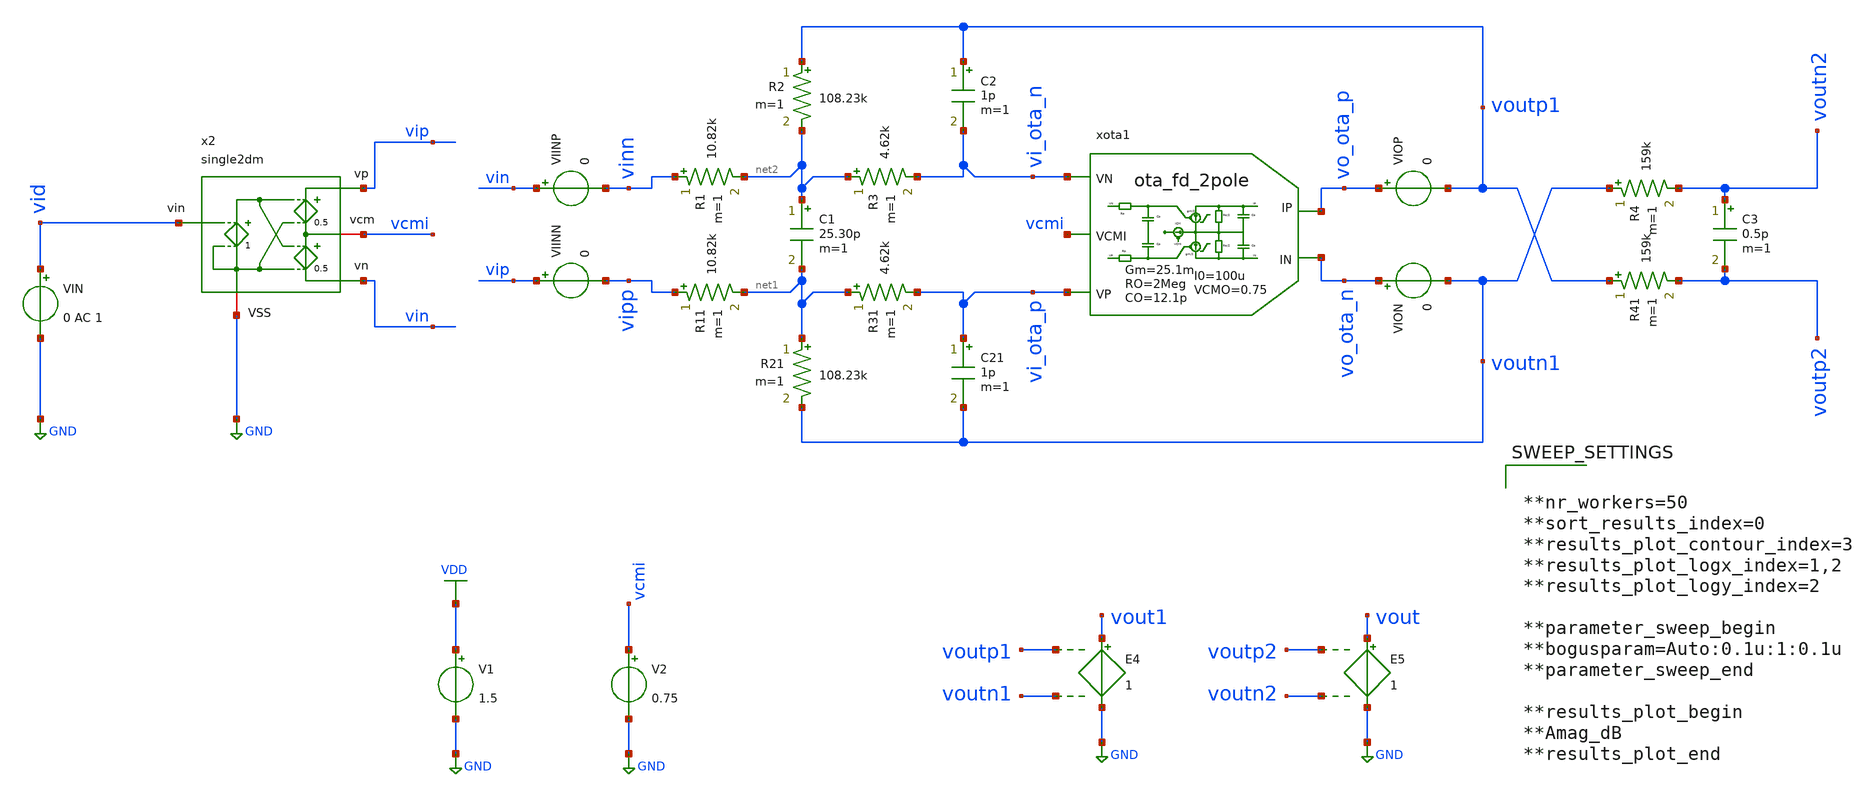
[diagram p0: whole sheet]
** sch_path: macros/filter_cmos5l/testbenches/xschem/filter_cl_ideal_tb.sch
**.subckt filter_cl_ideal_tb
VIN vid GND 0 AC 1
E4 vout1 GND voutp1 voutn1 1
VIINP vin vinn 0
VIINN vip vipp 0
R1 vinn net2 10.82k m=1
R2 voutp1 net2 108.23k m=1
R3 net2 vi_ota_n 4.62k m=1
C1 net2 net1 25.30p m=1
C3 voutn2 voutp2 0.5p m=1
R11 vipp net1 10.82k m=1
R21 net1 voutn1 108.23k m=1
R31 net1 vi_ota_p 4.62k m=1
C21 vi_ota_p voutn1 1p m=1
R4 voutn1 voutn2 159k m=1
R41 voutp1 voutp2 159k m=1
C2 voutp1 vi_ota_n 1p m=1
E5 vout GND voutp2 voutn2 1
VIOP vo_ota_p voutp1 0
VION vo_ota_n voutn1 0
V1 VDD GND 1.5
x2 vip vid vcmi GND vin single2dm
V2 vcmi GND 0.75
xota1 vi_ota_n vo_ota_p vo_ota_n vi_ota_p vcmi ota_fd_2pole GM=25.1m RO=2Meg CO=12.1p RP=0 CP=0.1p
+ VCMO=0.75 I0=100u
**** begin user architecture code


.options savecurrents
.options method=gear reltol=.005
.options sparse
.control
save all

let f_min = 10
let f_max = 100Meg
let f_stop = 9Meg
let f_nmin = 100
let f_nmax = 5Meg

let n_bits = 8
let Adc = 10
let v_fs = 1.0
let v_lsb = v_fs/2^n_bits
let v_qn = v_lsb/sqrt(12)
let err_gain_spec = v_lsb/v_fs
let vo_n_max = 113e-6

let v_step_o = v_fs
let v_step_i = v_step_o/Adc

let t_rf = 0.1u
let t_step = 50u
let t_delay = 0
let t_per = 2*t_step

let tstep = 0.1*t_rf
let tstop = 2*t_per
let tstart = t_delay

*alter @VIN[SIN] = [ 0 0.01 $&f_sig 0 0 0 ]
alter @VIN[DC] = 0.0

set wr_singlescale
set wr_vecnames
option numdgt=3

set opSimOnly = 0


** Main Simulations
if $opSimOnly eq 0
	op
	ac dec 100 $&const.f_min $&const.f_max
	*set sqrnoise
	noise v(vout) VIN dec 100 $&const.f_min $&const.f_max 1
	noise v(vout) VIN dec 10 $&const.f_nmin $&const.f_nmax
	alter @VIN[PULSE] = [ 0 $&v_step_i $&t_delay $&t_rf $&t_rf $&t_step $&t_per 0 ]
	** Check power on by ramping Vdd, tie di_pon to VDD net!
	*alter @V1[PULSE] = [ 0 1.8 0 10u $&t_rf 0 0 0 ]
	tran $&tstep $&tstop $&tstart

	setplot ac1
	let A1 = v(vout1)/v(vid)
	let A2 = v(vout)/v(vid)

	let Amag_dB = vdb(A2)
	settype decibel Amag_dB
	let Aarg = 180/PI*cphase(A2)
	echo results_plot_begin
	print Amag_dB
	echo results_plot_end
	let fdc = const.f_min+1
	meas ac Adc_ol_dB find Amag_dB when frequency = fdc
	let Amag_fc = Adc_ol_dB-3
	meas ac fc find frequency when Amag_dB = Amag_fc
	meas ac Amin min_at Amag_dB from=const.f_min to=fc
	meas ac Amax max Amag_dB
	meas ac Astop find Amag_dB when frequency = const.f_stop
	let att_db = Adc_ol_dB-Astop

	meas ac fug find frequency when Amag_dB=0
	let err_gain_act = 1-10^(Adc_ol_dB/20)/Adc
	let Adc_ol_min = (1+Adc)*(1-err_gain_spec)/err_gain_spec
	let Adc_ol_min_dB = vdb(Adc_ol_min)
	print err_gain_act*100
	print Adc_ol_min_dB
	print att_db
	wrdata ../plot_simulations/data/filter_cl_ideal_tb_ac.txt Amag_dB Aarg
	plot Amag_dB Aarg ylabel 'Magnitude, Phase'

	setplot noise3
	wrdata ../plot_simulations/data/filter_cl_ideal_tb_noise.txt onoise_spectrum

	setplot noise4
	let p_noise_q = const.v_qn^2
	let p_noise_o = onoise_total^2
	let p_sig_o = (v_step_o/(2*sqrt(2)))^2
	let snr = p_sig_o/(p_noise_o+p_noise_q)
	let snr_dB = 10*log10(snr)
	print snr_dB

	setplot tran4
	let vid = v(vid)
	let iop = viop#branch
	let ion = vion#branch
	let vcmo = (voutp1+voutn1)/2

	*plot iop ion

	*plot vid vout1 vout vcmo
	*plot v(vip) v(vin) v(voutp1) v(voutn1) vcmo
end

alter @VIN[DC] = 0
op

remzerovec
write filter_cl_ideal_tb.raw
.endc



**nr_workers=50
**sort_results_index=0
**results_plot_contour_index=3
**results_plot_logx_index=1,2
**results_plot_logy_index=2

**parameter_sweep_begin
**bogusparam=Auto:0.1u:1:0.1u
**parameter_sweep_end

**results_plot_begin
**Amag_dB
**results_plot_end


**** end user architecture code
**.ends

* expanding   symbol:  single2dm.sym # of pins=5
** sym_path: single2dm.sym
** sch_path: single2dm.sch
.subckt single2dm vp vin vcm VSS vn
*.ipin vin
*.opin vn
*.iopin vcm
*.opin vp
*.iopin VSS
E3 vcm vn net1 VSS 0.5
E2 vp vcm net1 VSS 0.5
E1 net1 VSS vin VSS 1
.ends


* expanding   symbol:  ota_fd_2pole.sym # of pins=5
** sym_path: ota_fd_2pole.sym
** sch_path: ota_fd_2pole.sch
.subckt ota_fd_2pole VN IP IN VP VCMI  GM=1u RO=100Meg CO=1p RP=0 CP=0.1p VCMO=0 I0=1u
*.ipin VP
*.ipin VN
*.opin IP
*.opin IN
*.ipin VCMI
R3 IP net1 {RO/2} m=1
R4 IN net1 {RO/2} m=1
C3 IP net1 {CO} m=1
R5 VN ip1 {RP} m=1
C4 ip1 VCMI {CP} m=1
C6 in1 VCMI {CP} m=1
C8 IN net1 {CO} m=1
R7 VP in1 {RP} m=1
B2 IP net1 I = {I0*tanh(GM/2*V(ip1,in1)/I0)}
B1 net1 IN I = {I0*tanh(GM/2*V(ip1,in1)/I0)}
B5 net1 GND I = {VCMO-(V(IP)+V(IN))/2}
.ends

.GLOBAL GND
.GLOBAL VDD
.end
